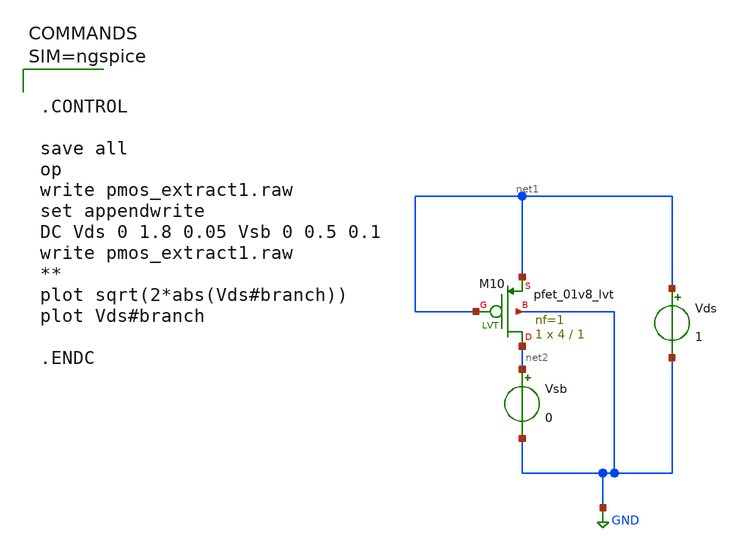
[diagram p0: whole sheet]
** sch_path: work/xschem/pmos_extract1.sch
**.subckt pmos_extract1
Vds net1 GND 1
Vsb net2 GND 0
XM10 net2 net1 net1 GND sky130_fd_pr__pfet_01v8_lvt L=1 W=4 nf=1 ad='int((1 + 1)/2) * 4 / 1 * 0.29' as='int((1 + 2)/2) * 4 / 1 * 0.29'
+ pd='2*int((1 + 1)/2) * (4 / 1 + 0.29)' ps='2*int((1 + 2)/2) * (4 / 1 + 0.29)' nrd='0.29 / 4 ' nrs='0.29 / 4 '
+ sa=0 sb=0 sd=0 mult=1 m=1
**** begin user architecture code



.CONTROL

save all
op
write pmos_extract1.raw
set appendwrite
DC Vds 0 1.8 0.05 Vsb 0 0.5 0.1
write pmos_extract1.raw
**
plot sqrt(2*abs(Vds#branch))
plot Vds#branch

.ENDC




** opencircuitdesign pdks install
.lib $::SKYWATER_MODELS/sky130.lib.spice tt

**** end user architecture code
**.ends
.GLOBAL GND
.end
